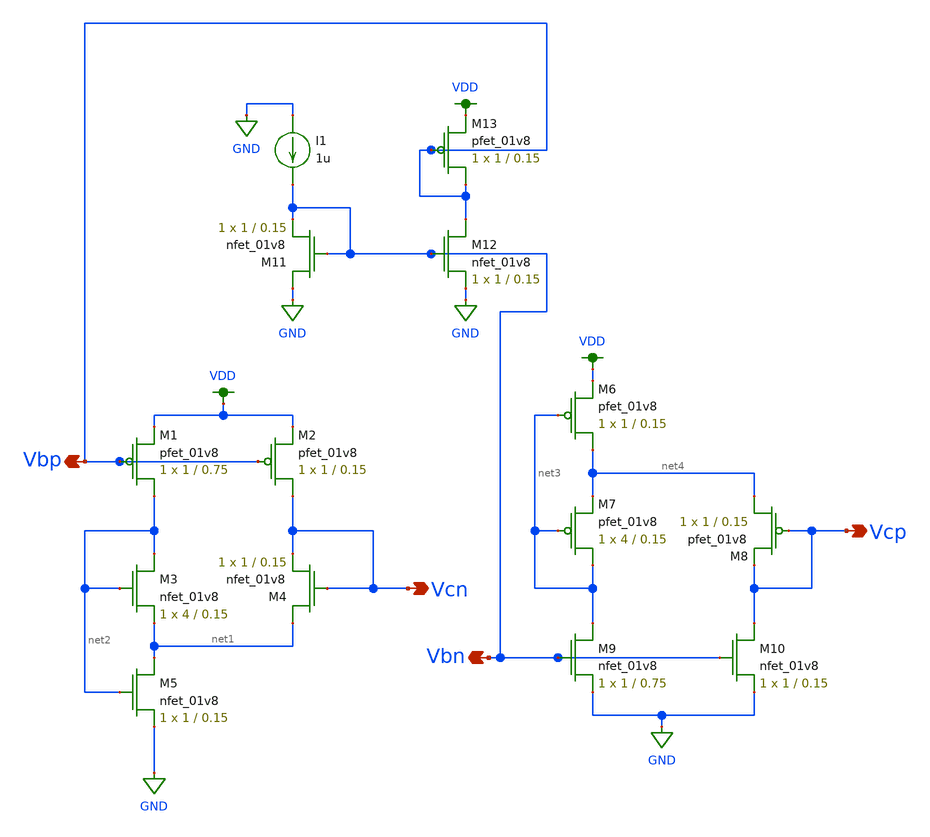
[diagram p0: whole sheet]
** sch_path: miniproject3/bias_generator.sch
**.subckt bias_generator Vbp Vbn Vcp Vcn
*.opin Vbp
*.opin Vbn
*.opin Vcp
*.opin Vcn
XM1 net2 Vbp VDD VDD sky130_fd_pr__pfet_01v8 L=0.75 W=1 nf=1 ad='int((nf+1)/2) * W/nf * 0.29' as='int((nf+2)/2) * W/nf * 0.29'
+ pd='2*int((nf+1)/2) * (W/nf + 0.29)' ps='2*int((nf+2)/2) * (W/nf + 0.29)' nrd='0.29 / W' nrs='0.29 / W'
+ sa=0 sb=0 sd=0 mult=1 m=1
XM2 Vcn Vbp VDD VDD sky130_fd_pr__pfet_01v8 L=0.15 W=1 nf=1 ad='int((nf+1)/2) * W/nf * 0.29' as='int((nf+2)/2) * W/nf * 0.29'
+ pd='2*int((nf+1)/2) * (W/nf + 0.29)' ps='2*int((nf+2)/2) * (W/nf + 0.29)' nrd='0.29 / W' nrs='0.29 / W'
+ sa=0 sb=0 sd=0 mult=1 m=1
XM3 net2 net2 net1 GND sky130_fd_pr__nfet_01v8 L=0.15 W=4 nf=1 ad='int((nf+1)/2) * W/nf * 0.29' as='int((nf+2)/2) * W/nf * 0.29'
+ pd='2*int((nf+1)/2) * (W/nf + 0.29)' ps='2*int((nf+2)/2) * (W/nf + 0.29)' nrd='0.29 / W' nrs='0.29 / W'
+ sa=0 sb=0 sd=0 mult=1 m=1
XM4 net1 Vcn Vcn GND sky130_fd_pr__nfet_01v8 L=0.15 W=1 nf=1 ad='int((nf+1)/2) * W/nf * 0.29' as='int((nf+2)/2) * W/nf * 0.29'
+ pd='2*int((nf+1)/2) * (W/nf + 0.29)' ps='2*int((nf+2)/2) * (W/nf + 0.29)' nrd='0.29 / W' nrs='0.29 / W'
+ sa=0 sb=0 sd=0 mult=1 m=1
XM5 net1 net2 GND GND sky130_fd_pr__nfet_01v8 L=0.15 W=1 nf=1 ad='int((nf+1)/2) * W/nf * 0.29' as='int((nf+2)/2) * W/nf * 0.29'
+ pd='2*int((nf+1)/2) * (W/nf + 0.29)' ps='2*int((nf+2)/2) * (W/nf + 0.29)' nrd='0.29 / W' nrs='0.29 / W'
+ sa=0 sb=0 sd=0 mult=1 m=1
XM6 net4 net3 VDD VDD sky130_fd_pr__pfet_01v8 L=0.15 W=1 nf=1 ad='int((nf+1)/2) * W/nf * 0.29' as='int((nf+2)/2) * W/nf * 0.29'
+ pd='2*int((nf+1)/2) * (W/nf + 0.29)' ps='2*int((nf+2)/2) * (W/nf + 0.29)' nrd='0.29 / W' nrs='0.29 / W'
+ sa=0 sb=0 sd=0 mult=1 m=1
XM7 net3 net3 net4 VDD sky130_fd_pr__pfet_01v8 L=0.15 W=4 nf=1 ad='int((nf+1)/2) * W/nf * 0.29' as='int((nf+2)/2) * W/nf * 0.29'
+ pd='2*int((nf+1)/2) * (W/nf + 0.29)' ps='2*int((nf+2)/2) * (W/nf + 0.29)' nrd='0.29 / W' nrs='0.29 / W'
+ sa=0 sb=0 sd=0 mult=1 m=1
XM8 net4 Vcp Vcp VDD sky130_fd_pr__pfet_01v8 L=0.15 W=1 nf=1 ad='int((nf+1)/2) * W/nf * 0.29' as='int((nf+2)/2) * W/nf * 0.29'
+ pd='2*int((nf+1)/2) * (W/nf + 0.29)' ps='2*int((nf+2)/2) * (W/nf + 0.29)' nrd='0.29 / W' nrs='0.29 / W'
+ sa=0 sb=0 sd=0 mult=1 m=1
XM9 net3 Vbn GND GND sky130_fd_pr__nfet_01v8 L=0.75 W=1 nf=1 ad='int((nf+1)/2) * W/nf * 0.29' as='int((nf+2)/2) * W/nf * 0.29'
+ pd='2*int((nf+1)/2) * (W/nf + 0.29)' ps='2*int((nf+2)/2) * (W/nf + 0.29)' nrd='0.29 / W' nrs='0.29 / W'
+ sa=0 sb=0 sd=0 mult=1 m=1
XM10 Vcp Vbn GND GND sky130_fd_pr__nfet_01v8 L=0.15 W=1 nf=1 ad='int((nf+1)/2) * W/nf * 0.29' as='int((nf+2)/2) * W/nf * 0.29'
+ pd='2*int((nf+1)/2) * (W/nf + 0.29)' ps='2*int((nf+2)/2) * (W/nf + 0.29)' nrd='0.29 / W' nrs='0.29 / W'
+ sa=0 sb=0 sd=0 mult=1 m=1
I1 GND Vbn 1u
XM11 GND Vbn Vbn GND sky130_fd_pr__nfet_01v8 L=0.15 W=1 nf=1 ad='int((nf+1)/2) * W/nf * 0.29' as='int((nf+2)/2) * W/nf * 0.29'
+ pd='2*int((nf+1)/2) * (W/nf + 0.29)' ps='2*int((nf+2)/2) * (W/nf + 0.29)' nrd='0.29 / W' nrs='0.29 / W'
+ sa=0 sb=0 sd=0 mult=1 m=1
XM12 Vbp Vbn GND GND sky130_fd_pr__nfet_01v8 L=0.15 W=1 nf=1 ad='int((nf+1)/2) * W/nf * 0.29' as='int((nf+2)/2) * W/nf * 0.29'
+ pd='2*int((nf+1)/2) * (W/nf + 0.29)' ps='2*int((nf+2)/2) * (W/nf + 0.29)' nrd='0.29 / W' nrs='0.29 / W'
+ sa=0 sb=0 sd=0 mult=1 m=1
XM13 Vbp Vbp VDD VDD sky130_fd_pr__pfet_01v8 L=0.15 W=1 nf=1 ad='int((nf+1)/2) * W/nf * 0.29' as='int((nf+2)/2) * W/nf * 0.29'
+ pd='2*int((nf+1)/2) * (W/nf + 0.29)' ps='2*int((nf+2)/2) * (W/nf + 0.29)' nrd='0.29 / W' nrs='0.29 / W'
+ sa=0 sb=0 sd=0 mult=1 m=1
**.ends
.GLOBAL VDD
.GLOBAL GND
.end
